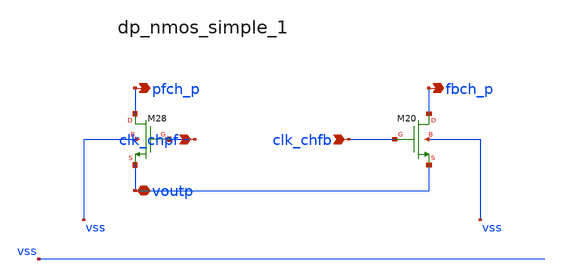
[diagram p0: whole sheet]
** sch_path: analog-db/raw/ia_003_fan_chopper_pf/hier/blocks/dp_nmos_simple_1.sch
**.subckt dp_nmos_simple_1 clk_chpf clk_chfb voutp pfch_p fbch_p
*.ipin clk_chpf
*.ipin clk_chfb
*.iopin voutp
*.opin pfch_p
*.opin fbch_p
XM20 fbch_p clk_chfb voutp vss sg13_lv_nmos w=x_dut_xm20_w l=x_dut_xm20_l ng=1 m=x_dut_xm20_m
XM28 pfch_p clk_chpf voutp vss sg13_lv_nmos w=x_dut_xm28_w l=x_dut_xm28_l ng=1 m=x_dut_xm28_m
**.ends
.end
